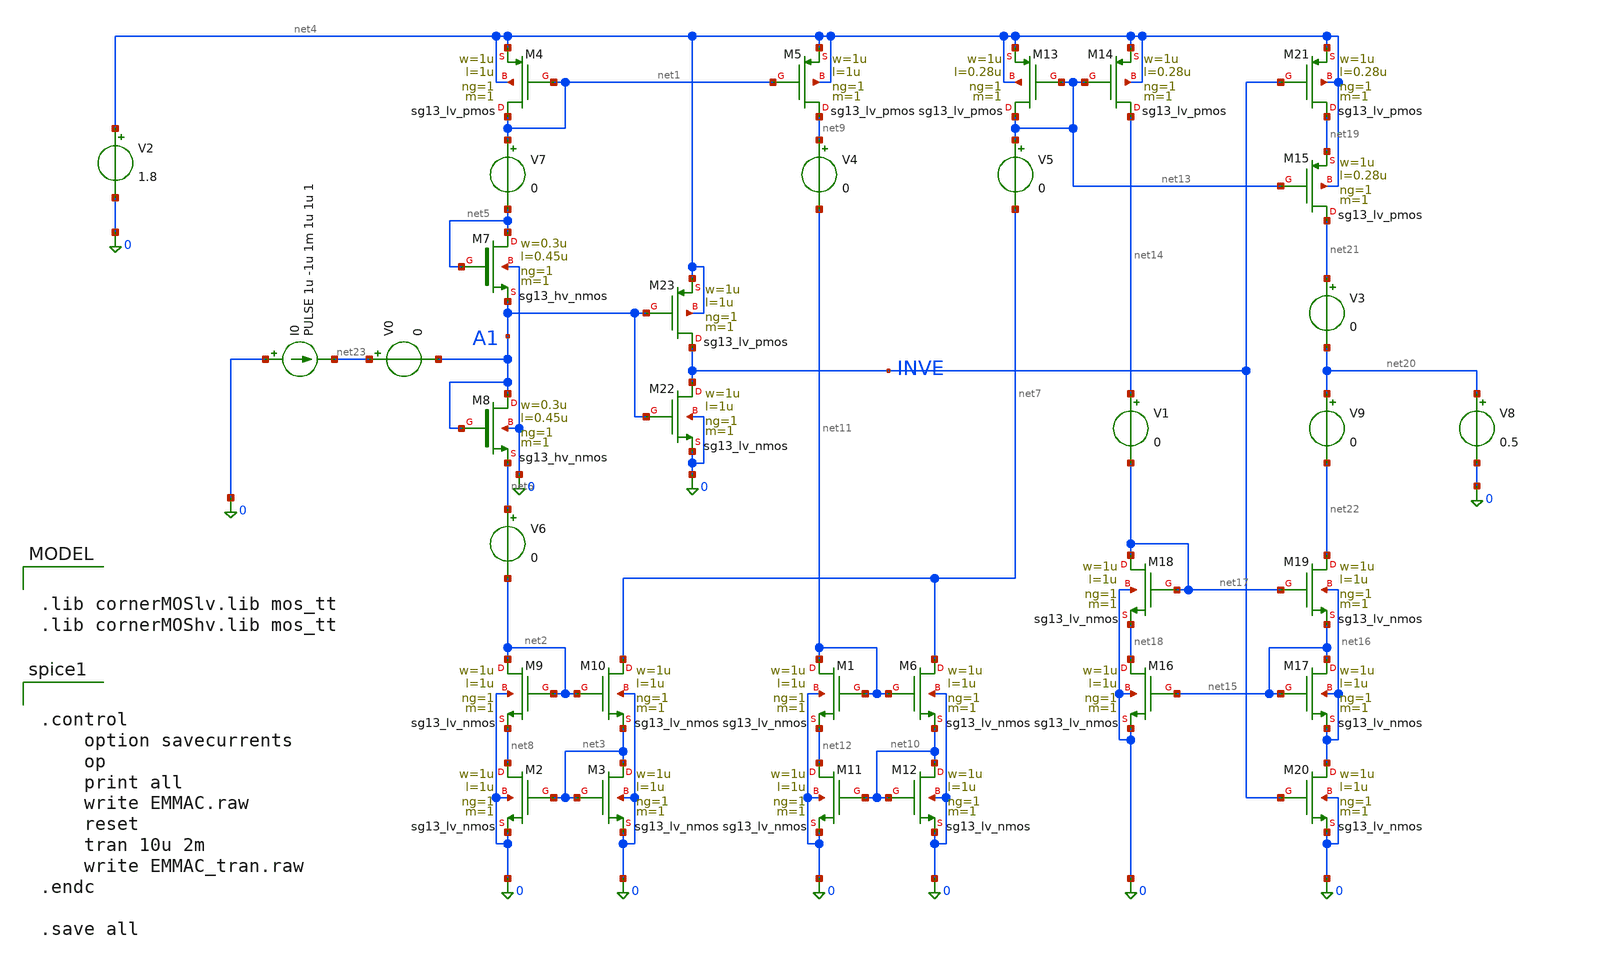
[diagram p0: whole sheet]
** sch_path: src/analog_mac/EMMAC.sch
**.subckt EMMAC
V2 net4 0 1.8
I0 0 net23 PULSE 1u -1u 1m 1u 1u 1
V6 net6 net2 0
V7 net1 net5 0
XM2 net8 net3 0 0 sg13_lv_nmos w=1u l=1u ng=1 m=1 mm_ok=1
XM3 net3 net3 0 0 sg13_lv_nmos w=1u l=1u ng=1 m=1 mm_ok=1
XM4 net1 net1 net4 net4 sg13_lv_pmos w=1u l=1u ng=1 m=1 mm_ok=1
XM5 net9 net1 net4 net4 sg13_lv_pmos w=1u l=1u ng=1 m=1 mm_ok=1
V4 net9 net11 0
V5 net13 net7 0
XM9 net2 net2 net8 0 sg13_lv_nmos w=1u l=1u ng=1 m=1 mm_ok=1
XM10 net7 net2 net3 0 sg13_lv_nmos w=1u l=1u ng=1 m=1 mm_ok=1
XM11 net12 net10 0 0 sg13_lv_nmos w=1u l=1u ng=1 m=1 mm_ok=1
XM12 net10 net10 0 0 sg13_lv_nmos w=1u l=1u ng=1 m=1 mm_ok=1
XM1 net11 net11 net12 0 sg13_lv_nmos w=1u l=1u ng=1 m=1 mm_ok=1
XM6 net7 net11 net10 0 sg13_lv_nmos w=1u l=1u ng=1 m=1 mm_ok=1
XM13 net13 net13 net4 net4 sg13_lv_pmos w=1u l=0.28u ng=1 m=1 mm_ok=1
XM14 net14 net13 net4 net4 sg13_lv_pmos w=1u l=0.28u ng=1 m=1 mm_ok=1
V1 net14 net17 0
XM7 net5 net5 A1 0 sg13_hv_nmos w=0.3u l=0.45u ng=1 m=1 mm_ok=1
XM8 A1 A1 net6 0 sg13_hv_nmos w=0.3u l=0.45u ng=1 m=1 mm_ok=1
XM15 net21 net13 net19 net4 sg13_lv_pmos w=1u l=0.28u ng=1 m=1 mm_ok=1
V3 net21 net20 0
XM16 net18 net15 0 0 sg13_lv_nmos w=1u l=1u ng=1 m=1 mm_ok=1
XM17 net15 net15 net16 net16 sg13_lv_nmos w=1u l=1u ng=1 m=1 mm_ok=1
XM18 net17 net17 net18 0 sg13_lv_nmos w=1u l=1u ng=1 m=1 mm_ok=1
XM19 net22 net17 net15 net16 sg13_lv_nmos w=1u l=1u ng=1 m=1 mm_ok=1
XM20 net16 INVE 0 0 sg13_lv_nmos w=1u l=1u ng=1 m=1 mm_ok=1
XM21 net19 INVE net4 net4 sg13_lv_pmos w=1u l=0.28u ng=1 m=1 mm_ok=1
XM22 INVE A1 0 0 sg13_lv_nmos w=1u l=1u ng=1 m=1 mm_ok=1
XM23 INVE A1 net4 net4 sg13_lv_pmos w=1u l=1u ng=1 m=1 mm_ok=1
V8 net20 0 0.5
V9 net20 net22 0
V0 net23 A1 0
**** begin user architecture code

.lib cornerMOSlv.lib mos_tt
.lib cornerMOShv.lib mos_tt



.control
	option savecurrents
	op
	print all
	write EMMAC.raw
	reset
	tran 10u 2m
	write EMMAC_tran.raw
.endc

.save all


**** end user architecture code
**.ends
.end
